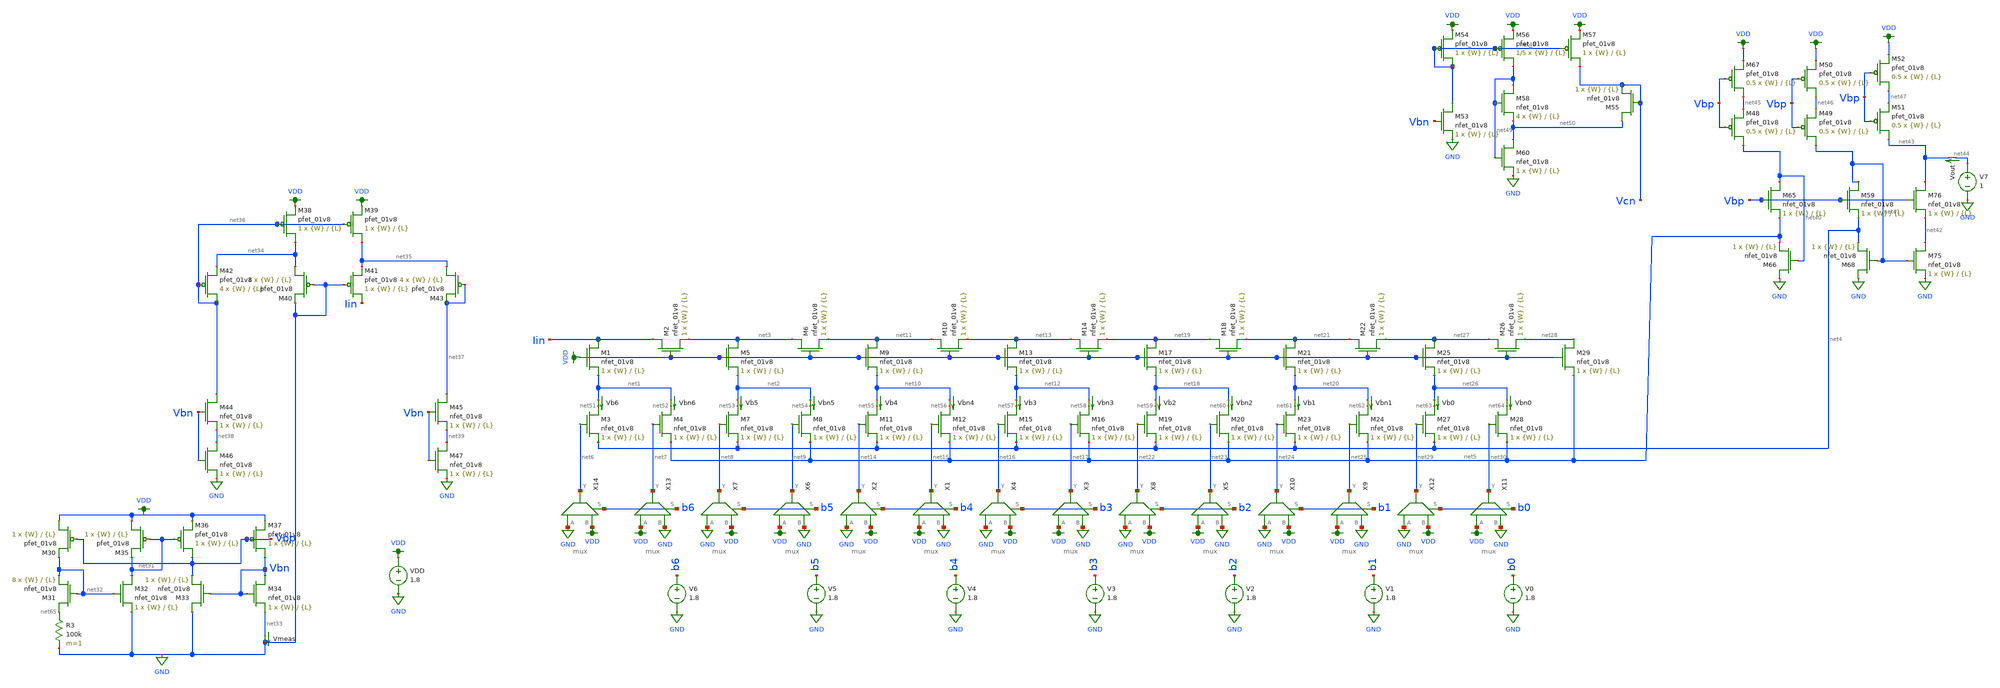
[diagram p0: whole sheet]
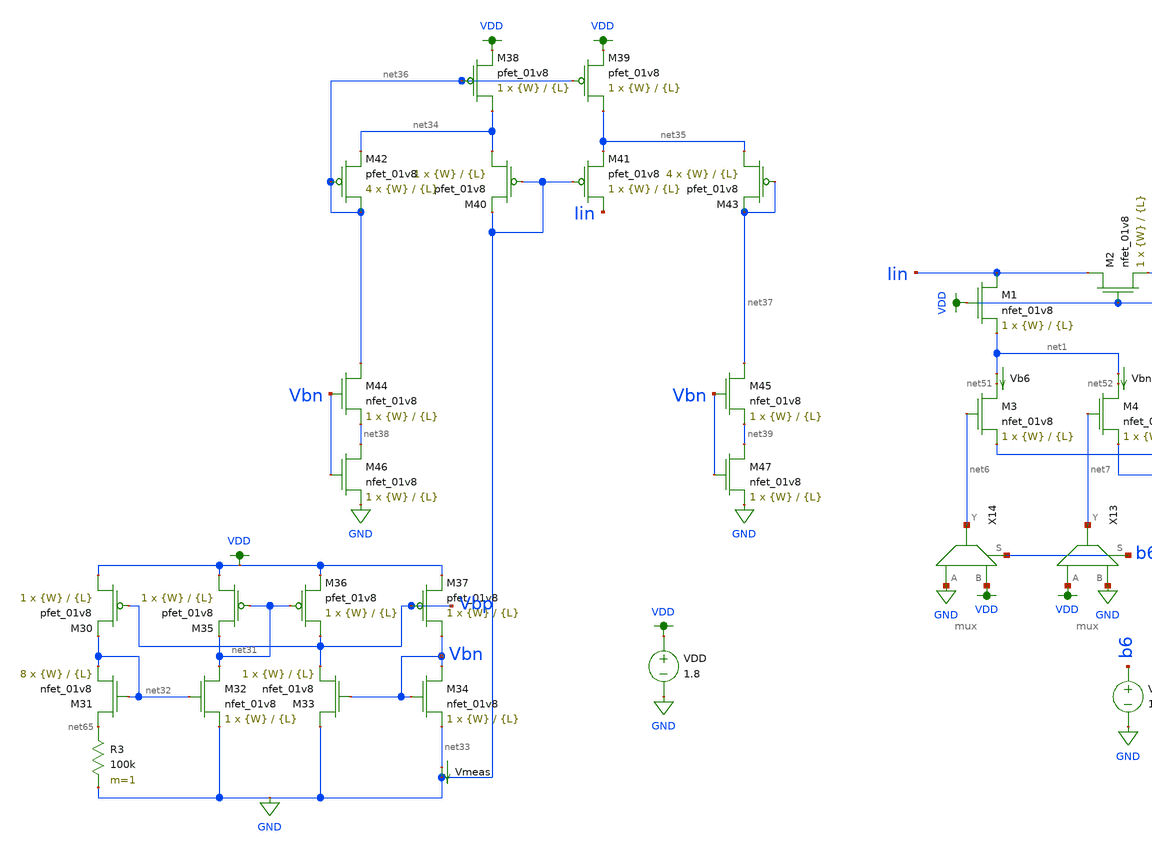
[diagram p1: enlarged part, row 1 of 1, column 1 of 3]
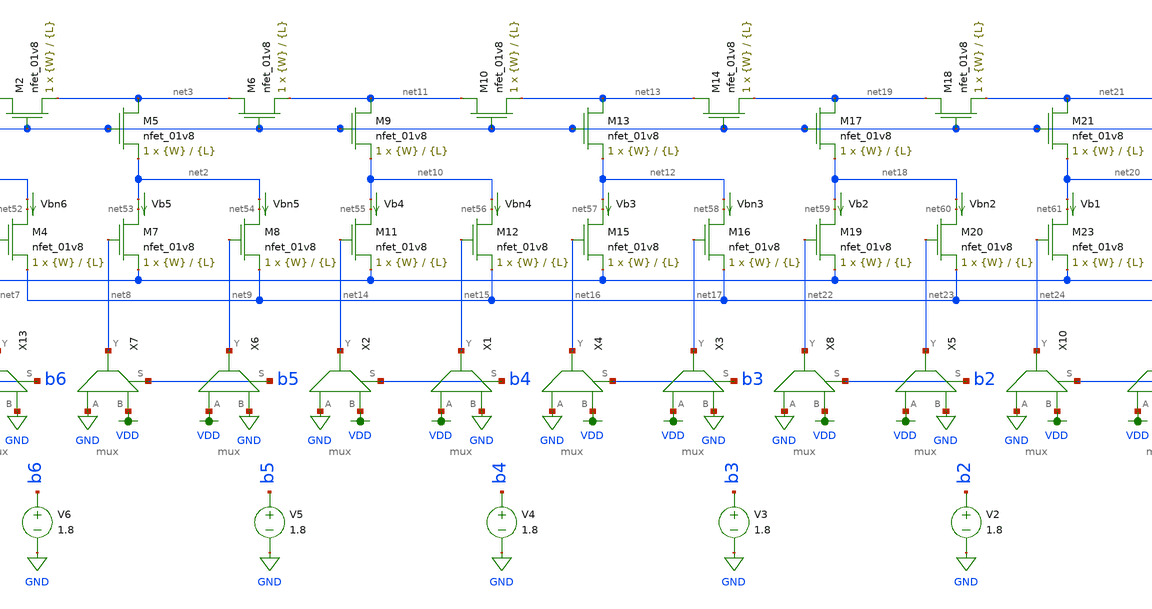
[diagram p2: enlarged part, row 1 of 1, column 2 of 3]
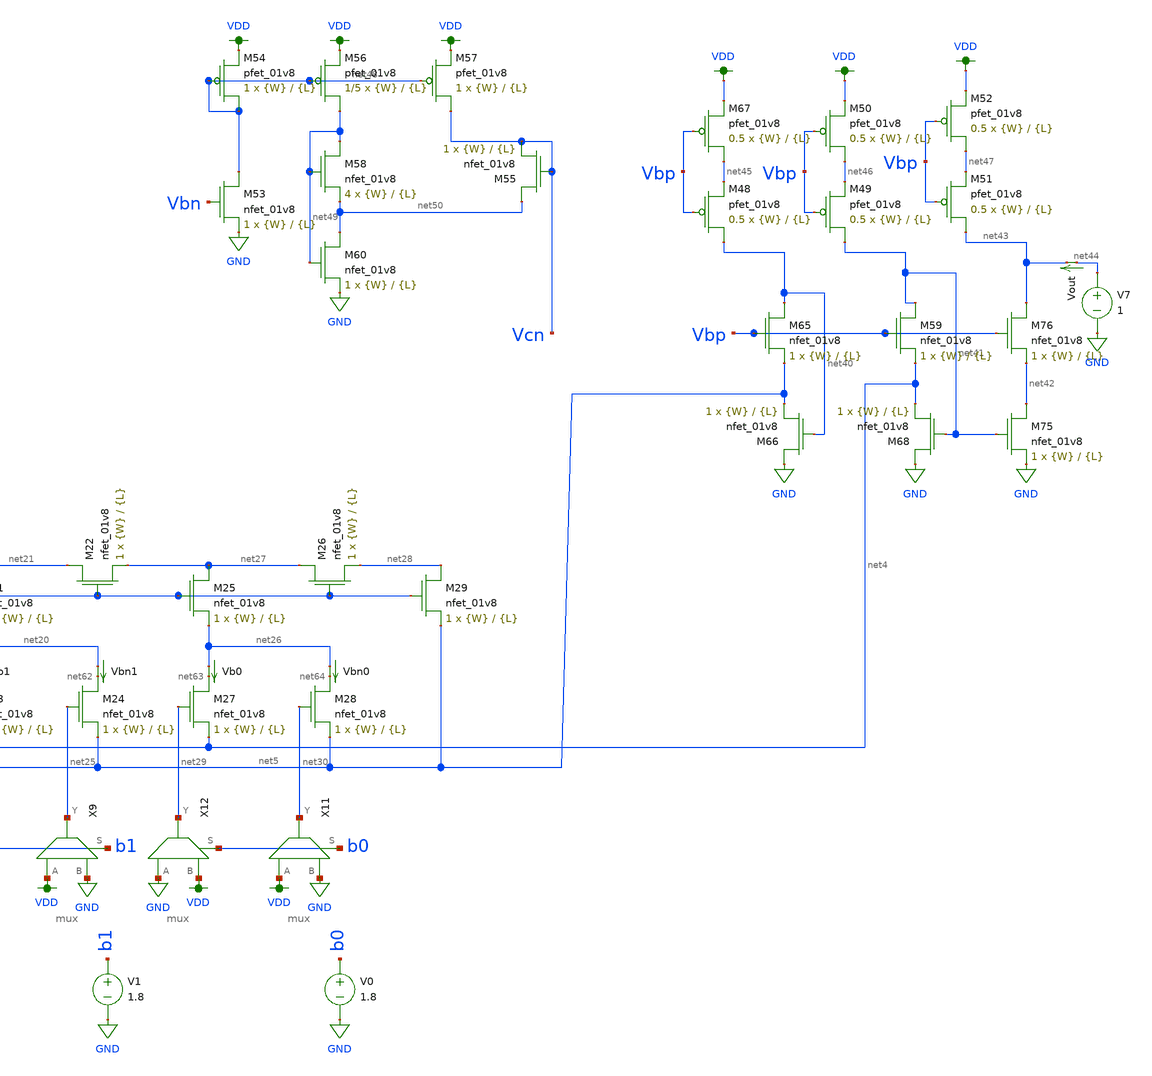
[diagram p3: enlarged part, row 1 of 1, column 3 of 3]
** sch_path: schematics/dac_from_paper_2.sch
**.subckt dac_from_paper_2
XM1 Iin VDD net1 GND sky130_fd_pr__nfet_01v8 L={L} W={W} nf=1 ad='int((nf+1)/2) * W/nf * 0.29' as='int((nf+2)/2) * W/nf * 0.29'
+ pd='2*int((nf+1)/2) * (W/nf + 0.29)' ps='2*int((nf+2)/2) * (W/nf + 0.29)' nrd='0.29 / W' nrs='0.29 / W'
+ sa=0 sb=0 sd=0 mult=1 m=1
XM2 Iin VDD net3 GND sky130_fd_pr__nfet_01v8 L={L} W={W} nf=1 ad='int((nf+1)/2) * W/nf * 0.29' as='int((nf+2)/2) * W/nf * 0.29'
+ pd='2*int((nf+1)/2) * (W/nf + 0.29)' ps='2*int((nf+2)/2) * (W/nf + 0.29)' nrd='0.29 / W' nrs='0.29 / W'
+ sa=0 sb=0 sd=0 mult=1 m=1
XM3 net51 net6 net4 GND sky130_fd_pr__nfet_01v8 L={L} W={W} nf=1 ad='int((nf+1)/2) * W/nf * 0.29' as='int((nf+2)/2) * W/nf * 0.29'
+ pd='2*int((nf+1)/2) * (W/nf + 0.29)' ps='2*int((nf+2)/2) * (W/nf + 0.29)' nrd='0.29 / W' nrs='0.29 / W'
+ sa=0 sb=0 sd=0 mult=1 m=1
XM4 net52 net7 net5 GND sky130_fd_pr__nfet_01v8 L={L} W={W} nf=1 ad='int((nf+1)/2) * W/nf * 0.29' as='int((nf+2)/2) * W/nf * 0.29'
+ pd='2*int((nf+1)/2) * (W/nf + 0.29)' ps='2*int((nf+2)/2) * (W/nf + 0.29)' nrd='0.29 / W' nrs='0.29 / W'
+ sa=0 sb=0 sd=0 mult=1 m=1
XM5 net3 VDD net2 GND sky130_fd_pr__nfet_01v8 L={L} W={W} nf=1 ad='int((nf+1)/2) * W/nf * 0.29' as='int((nf+2)/2) * W/nf * 0.29'
+ pd='2*int((nf+1)/2) * (W/nf + 0.29)' ps='2*int((nf+2)/2) * (W/nf + 0.29)' nrd='0.29 / W' nrs='0.29 / W'
+ sa=0 sb=0 sd=0 mult=1 m=1
XM6 net3 VDD net11 GND sky130_fd_pr__nfet_01v8 L={L} W={W} nf=1 ad='int((nf+1)/2) * W/nf * 0.29' as='int((nf+2)/2) * W/nf * 0.29'
+ pd='2*int((nf+1)/2) * (W/nf + 0.29)' ps='2*int((nf+2)/2) * (W/nf + 0.29)' nrd='0.29 / W' nrs='0.29 / W'
+ sa=0 sb=0 sd=0 mult=1 m=1
XM7 net53 net8 net4 GND sky130_fd_pr__nfet_01v8 L={L} W={W} nf=1 ad='int((nf+1)/2) * W/nf * 0.29' as='int((nf+2)/2) * W/nf * 0.29'
+ pd='2*int((nf+1)/2) * (W/nf + 0.29)' ps='2*int((nf+2)/2) * (W/nf + 0.29)' nrd='0.29 / W' nrs='0.29 / W'
+ sa=0 sb=0 sd=0 mult=1 m=1
XM8 net54 net9 net5 GND sky130_fd_pr__nfet_01v8 L={L} W={W} nf=1 ad='int((nf+1)/2) * W/nf * 0.29' as='int((nf+2)/2) * W/nf * 0.29'
+ pd='2*int((nf+1)/2) * (W/nf + 0.29)' ps='2*int((nf+2)/2) * (W/nf + 0.29)' nrd='0.29 / W' nrs='0.29 / W'
+ sa=0 sb=0 sd=0 mult=1 m=1
XM9 net11 VDD net10 GND sky130_fd_pr__nfet_01v8 L={L} W={W} nf=1 ad='int((nf+1)/2) * W/nf * 0.29' as='int((nf+2)/2) * W/nf * 0.29'
+ pd='2*int((nf+1)/2) * (W/nf + 0.29)' ps='2*int((nf+2)/2) * (W/nf + 0.29)' nrd='0.29 / W' nrs='0.29 / W'
+ sa=0 sb=0 sd=0 mult=1 m=1
XM10 net11 VDD net13 GND sky130_fd_pr__nfet_01v8 L={L} W={W} nf=1 ad='int((nf+1)/2) * W/nf * 0.29' as='int((nf+2)/2) * W/nf * 0.29'
+ pd='2*int((nf+1)/2) * (W/nf + 0.29)' ps='2*int((nf+2)/2) * (W/nf + 0.29)' nrd='0.29 / W' nrs='0.29 / W'
+ sa=0 sb=0 sd=0 mult=1 m=1
XM11 net55 net14 net4 GND sky130_fd_pr__nfet_01v8 L={L} W={W} nf=1 ad='int((nf+1)/2) * W/nf * 0.29' as='int((nf+2)/2) * W/nf * 0.29'
+ pd='2*int((nf+1)/2) * (W/nf + 0.29)' ps='2*int((nf+2)/2) * (W/nf + 0.29)' nrd='0.29 / W' nrs='0.29 / W'
+ sa=0 sb=0 sd=0 mult=1 m=1
XM12 net56 net15 net5 GND sky130_fd_pr__nfet_01v8 L={L} W={W} nf=1 ad='int((nf+1)/2) * W/nf * 0.29' as='int((nf+2)/2) * W/nf * 0.29'
+ pd='2*int((nf+1)/2) * (W/nf + 0.29)' ps='2*int((nf+2)/2) * (W/nf + 0.29)' nrd='0.29 / W' nrs='0.29 / W'
+ sa=0 sb=0 sd=0 mult=1 m=1
XM13 net13 VDD net12 GND sky130_fd_pr__nfet_01v8 L={L} W={W} nf=1 ad='int((nf+1)/2) * W/nf * 0.29' as='int((nf+2)/2) * W/nf * 0.29'
+ pd='2*int((nf+1)/2) * (W/nf + 0.29)' ps='2*int((nf+2)/2) * (W/nf + 0.29)' nrd='0.29 / W' nrs='0.29 / W'
+ sa=0 sb=0 sd=0 mult=1 m=1
XM14 net13 VDD net19 GND sky130_fd_pr__nfet_01v8 L={L} W={W} nf=1 ad='int((nf+1)/2) * W/nf * 0.29' as='int((nf+2)/2) * W/nf * 0.29'
+ pd='2*int((nf+1)/2) * (W/nf + 0.29)' ps='2*int((nf+2)/2) * (W/nf + 0.29)' nrd='0.29 / W' nrs='0.29 / W'
+ sa=0 sb=0 sd=0 mult=1 m=1
XM15 net57 net16 net4 GND sky130_fd_pr__nfet_01v8 L={L} W={W} nf=1 ad='int((nf+1)/2) * W/nf * 0.29' as='int((nf+2)/2) * W/nf * 0.29'
+ pd='2*int((nf+1)/2) * (W/nf + 0.29)' ps='2*int((nf+2)/2) * (W/nf + 0.29)' nrd='0.29 / W' nrs='0.29 / W'
+ sa=0 sb=0 sd=0 mult=1 m=1
XM16 net58 net17 net5 GND sky130_fd_pr__nfet_01v8 L={L} W={W} nf=1 ad='int((nf+1)/2) * W/nf * 0.29' as='int((nf+2)/2) * W/nf * 0.29'
+ pd='2*int((nf+1)/2) * (W/nf + 0.29)' ps='2*int((nf+2)/2) * (W/nf + 0.29)' nrd='0.29 / W' nrs='0.29 / W'
+ sa=0 sb=0 sd=0 mult=1 m=1
XM17 net19 VDD net18 GND sky130_fd_pr__nfet_01v8 L={L} W={W} nf=1 ad='int((nf+1)/2) * W/nf * 0.29' as='int((nf+2)/2) * W/nf * 0.29'
+ pd='2*int((nf+1)/2) * (W/nf + 0.29)' ps='2*int((nf+2)/2) * (W/nf + 0.29)' nrd='0.29 / W' nrs='0.29 / W'
+ sa=0 sb=0 sd=0 mult=1 m=1
XM18 net19 VDD net21 GND sky130_fd_pr__nfet_01v8 L={L} W={W} nf=1 ad='int((nf+1)/2) * W/nf * 0.29' as='int((nf+2)/2) * W/nf * 0.29'
+ pd='2*int((nf+1)/2) * (W/nf + 0.29)' ps='2*int((nf+2)/2) * (W/nf + 0.29)' nrd='0.29 / W' nrs='0.29 / W'
+ sa=0 sb=0 sd=0 mult=1 m=1
XM19 net59 net22 net4 GND sky130_fd_pr__nfet_01v8 L={L} W={W} nf=1 ad='int((nf+1)/2) * W/nf * 0.29' as='int((nf+2)/2) * W/nf * 0.29'
+ pd='2*int((nf+1)/2) * (W/nf + 0.29)' ps='2*int((nf+2)/2) * (W/nf + 0.29)' nrd='0.29 / W' nrs='0.29 / W'
+ sa=0 sb=0 sd=0 mult=1 m=1
XM20 net60 net23 net5 GND sky130_fd_pr__nfet_01v8 L={L} W={W} nf=1 ad='int((nf+1)/2) * W/nf * 0.29' as='int((nf+2)/2) * W/nf * 0.29'
+ pd='2*int((nf+1)/2) * (W/nf + 0.29)' ps='2*int((nf+2)/2) * (W/nf + 0.29)' nrd='0.29 / W' nrs='0.29 / W'
+ sa=0 sb=0 sd=0 mult=1 m=1
XM21 net21 VDD net20 GND sky130_fd_pr__nfet_01v8 L={L} W={W} nf=1 ad='int((nf+1)/2) * W/nf * 0.29' as='int((nf+2)/2) * W/nf * 0.29'
+ pd='2*int((nf+1)/2) * (W/nf + 0.29)' ps='2*int((nf+2)/2) * (W/nf + 0.29)' nrd='0.29 / W' nrs='0.29 / W'
+ sa=0 sb=0 sd=0 mult=1 m=1
XM22 net21 VDD net27 GND sky130_fd_pr__nfet_01v8 L={L} W={W} nf=1 ad='int((nf+1)/2) * W/nf * 0.29' as='int((nf+2)/2) * W/nf * 0.29'
+ pd='2*int((nf+1)/2) * (W/nf + 0.29)' ps='2*int((nf+2)/2) * (W/nf + 0.29)' nrd='0.29 / W' nrs='0.29 / W'
+ sa=0 sb=0 sd=0 mult=1 m=1
XM23 net61 net24 net4 GND sky130_fd_pr__nfet_01v8 L={L} W={W} nf=1 ad='int((nf+1)/2) * W/nf * 0.29' as='int((nf+2)/2) * W/nf * 0.29'
+ pd='2*int((nf+1)/2) * (W/nf + 0.29)' ps='2*int((nf+2)/2) * (W/nf + 0.29)' nrd='0.29 / W' nrs='0.29 / W'
+ sa=0 sb=0 sd=0 mult=1 m=1
XM24 net62 net25 net5 GND sky130_fd_pr__nfet_01v8 L={L} W={W} nf=1 ad='int((nf+1)/2) * W/nf * 0.29' as='int((nf+2)/2) * W/nf * 0.29'
+ pd='2*int((nf+1)/2) * (W/nf + 0.29)' ps='2*int((nf+2)/2) * (W/nf + 0.29)' nrd='0.29 / W' nrs='0.29 / W'
+ sa=0 sb=0 sd=0 mult=1 m=1
XM25 net27 VDD net26 GND sky130_fd_pr__nfet_01v8 L={L} W={W} nf=1 ad='int((nf+1)/2) * W/nf * 0.29' as='int((nf+2)/2) * W/nf * 0.29'
+ pd='2*int((nf+1)/2) * (W/nf + 0.29)' ps='2*int((nf+2)/2) * (W/nf + 0.29)' nrd='0.29 / W' nrs='0.29 / W'
+ sa=0 sb=0 sd=0 mult=1 m=1
XM26 net27 VDD net28 GND sky130_fd_pr__nfet_01v8 L={L} W={W} nf=1 ad='int((nf+1)/2) * W/nf * 0.29' as='int((nf+2)/2) * W/nf * 0.29'
+ pd='2*int((nf+1)/2) * (W/nf + 0.29)' ps='2*int((nf+2)/2) * (W/nf + 0.29)' nrd='0.29 / W' nrs='0.29 / W'
+ sa=0 sb=0 sd=0 mult=1 m=1
XM27 net63 net29 net4 GND sky130_fd_pr__nfet_01v8 L={L} W={W} nf=1 ad='int((nf+1)/2) * W/nf * 0.29' as='int((nf+2)/2) * W/nf * 0.29'
+ pd='2*int((nf+1)/2) * (W/nf + 0.29)' ps='2*int((nf+2)/2) * (W/nf + 0.29)' nrd='0.29 / W' nrs='0.29 / W'
+ sa=0 sb=0 sd=0 mult=1 m=1
XM28 net64 net30 net5 GND sky130_fd_pr__nfet_01v8 L={L} W={W} nf=1 ad='int((nf+1)/2) * W/nf * 0.29' as='int((nf+2)/2) * W/nf * 0.29'
+ pd='2*int((nf+1)/2) * (W/nf + 0.29)' ps='2*int((nf+2)/2) * (W/nf + 0.29)' nrd='0.29 / W' nrs='0.29 / W'
+ sa=0 sb=0 sd=0 mult=1 m=1
XM29 net28 VDD net5 GND sky130_fd_pr__nfet_01v8 L={L} W={W} nf=1 ad='int((nf+1)/2) * W/nf * 0.29' as='int((nf+2)/2) * W/nf * 0.29'
+ pd='2*int((nf+1)/2) * (W/nf + 0.29)' ps='2*int((nf+2)/2) * (W/nf + 0.29)' nrd='0.29 / W' nrs='0.29 / W'
+ sa=0 sb=0 sd=0 mult=1 m=1
Vb0 net26 net63 0
.save i(vb0)
Vbn0 net26 net64 0
.save i(vbn0)
Vb5 net2 net53 0
.save i(vb5)
Vb6 net1 net51 0
.save i(vb6)
Vb1 net20 net61 0
.save i(vb1)
Vb2 net18 net59 0
.save i(vb2)
Vb3 net12 net57 0
.save i(vb3)
Vb4 net10 net55 0
.save i(vb4)
Vbn1 net20 net62 0
.save i(vbn1)
Vbn2 net18 net60 0
.save i(vbn2)
Vbn3 net12 net58 0
.save i(vbn3)
Vbn4 net10 net56 0
.save i(vbn4)
Vbn5 net2 net54 0
.save i(vbn5)
Vbn6 net1 net52 0
.save i(vbn6)
V0 b0 GND 1.8
V1 b1 GND 1.8
V2 b2 GND 1.8
V3 b3 GND 1.8
V4 b4 GND 1.8
V5 b5 GND 1.8
V6 b6 GND 1.8
XM30 VDD Vbp net32 VDD sky130_fd_pr__pfet_01v8 L={L} W={W} nf=1 ad='int((nf+1)/2) * W/nf * 0.29' as='int((nf+2)/2) * W/nf * 0.29'
+ pd='2*int((nf+1)/2) * (W/nf + 0.29)' ps='2*int((nf+2)/2) * (W/nf + 0.29)' nrd='0.29 / W' nrs='0.29 / W'
+ sa=0 sb=0 sd=0 mult=1 m=1
XM31 net65 net32 net32 GND sky130_fd_pr__nfet_01v8 L={L} W={W} nf=1 ad='int((nf+1)/2) * W/nf * 0.29'
+ as='int((nf+2)/2) * W/nf * 0.29' pd='2*int((nf+1)/2) * (W/nf + 0.29)' ps='2*int((nf+2)/2) * (W/nf + 0.29)'
+ nrd='0.29 / W' nrs='0.29 / W' sa=0 sb=0 sd=0 mult=8 m=8
R3 net65 GND 100k m=1
XM32 net31 net32 GND GND sky130_fd_pr__nfet_01v8 L={L} W={W} nf=1 ad='int((nf+1)/2) * W/nf * 0.29' as='int((nf+2)/2) * W/nf * 0.29'
+ pd='2*int((nf+1)/2) * (W/nf + 0.29)' ps='2*int((nf+2)/2) * (W/nf + 0.29)' nrd='0.29 / W' nrs='0.29 / W'
+ sa=0 sb=0 sd=0 mult=1 m=1
XM33 GND Vbn Vbp GND sky130_fd_pr__nfet_01v8 L={L} W={W} nf=1 ad='int((nf+1)/2) * W/nf * 0.29' as='int((nf+2)/2) * W/nf * 0.29'
+ pd='2*int((nf+1)/2) * (W/nf + 0.29)' ps='2*int((nf+2)/2) * (W/nf + 0.29)' nrd='0.29 / W' nrs='0.29 / W'
+ sa=0 sb=0 sd=0 mult=1 m=1
XM34 Vbn Vbn net33 GND sky130_fd_pr__nfet_01v8 L={L} W={W} nf=1 ad='int((nf+1)/2) * W/nf * 0.29' as='int((nf+2)/2) * W/nf * 0.29'
+ pd='2*int((nf+1)/2) * (W/nf + 0.29)' ps='2*int((nf+2)/2) * (W/nf + 0.29)' nrd='0.29 / W' nrs='0.29 / W'
+ sa=0 sb=0 sd=0 mult=1 m=1
XM35 VDD net31 net31 VDD sky130_fd_pr__pfet_01v8 L={L} W={W} nf=1 ad='int((nf+1)/2) * W/nf * 0.29' as='int((nf+2)/2) * W/nf * 0.29'
+ pd='2*int((nf+1)/2) * (W/nf + 0.29)' ps='2*int((nf+2)/2) * (W/nf + 0.29)' nrd='0.29 / W' nrs='0.29 / W'
+ sa=0 sb=0 sd=0 mult=1 m=1
XM36 Vbp net31 VDD VDD sky130_fd_pr__pfet_01v8 L={L} W={W} nf=1 ad='int((nf+1)/2) * W/nf * 0.29' as='int((nf+2)/2) * W/nf * 0.29'
+ pd='2*int((nf+1)/2) * (W/nf + 0.29)' ps='2*int((nf+2)/2) * (W/nf + 0.29)' nrd='0.29 / W' nrs='0.29 / W'
+ sa=0 sb=0 sd=0 mult=1 m=1
XM37 Vbn Vbp VDD VDD sky130_fd_pr__pfet_01v8 L={L} W={W} nf=1 ad='int((nf+1)/2) * W/nf * 0.29' as='int((nf+2)/2) * W/nf * 0.29'
+ pd='2*int((nf+1)/2) * (W/nf + 0.29)' ps='2*int((nf+2)/2) * (W/nf + 0.29)' nrd='0.29 / W' nrs='0.29 / W'
+ sa=0 sb=0 sd=0 mult=1 m=1
VDD VDD GND 1.8
Vmeas net33 GND 0
.save i(vmeas)
X13 VDD GND net7 b6 mux
X14 GND VDD net6 b6 mux
X6 VDD GND net9 b5 mux
X7 GND VDD net8 b5 mux
X1 VDD GND net15 b4 mux
X2 GND VDD net14 b4 mux
X3 VDD GND net17 b3 mux
X4 GND VDD net16 b3 mux
X5 VDD GND net23 b2 mux
X8 GND VDD net22 b2 mux
X9 VDD GND net25 b1 mux
X10 GND VDD net24 b1 mux
X11 VDD GND net30 b0 mux
X12 GND VDD net29 b0 mux
XM38 net34 net36 VDD VDD sky130_fd_pr__pfet_01v8 L={L} W={W} nf=1 ad='int((nf+1)/2) * W/nf * 0.29' as='int((nf+2)/2) * W/nf * 0.29'
+ pd='2*int((nf+1)/2) * (W/nf + 0.29)' ps='2*int((nf+2)/2) * (W/nf + 0.29)' nrd='0.29 / W' nrs='0.29 / W'
+ sa=0 sb=0 sd=0 mult=1 m=1
XM39 net35 net36 VDD VDD sky130_fd_pr__pfet_01v8 L={L} W={W} nf=1 ad='int((nf+1)/2) * W/nf * 0.29' as='int((nf+2)/2) * W/nf * 0.29'
+ pd='2*int((nf+1)/2) * (W/nf + 0.29)' ps='2*int((nf+2)/2) * (W/nf + 0.29)' nrd='0.29 / W' nrs='0.29 / W'
+ sa=0 sb=0 sd=0 mult=1 m=1
XM40 net34 GND GND VDD sky130_fd_pr__pfet_01v8 L={L} W={W} nf=1 ad='int((nf+1)/2) * W/nf * 0.29' as='int((nf+2)/2) * W/nf * 0.29'
+ pd='2*int((nf+1)/2) * (W/nf + 0.29)' ps='2*int((nf+2)/2) * (W/nf + 0.29)' nrd='0.29 / W' nrs='0.29 / W'
+ sa=0 sb=0 sd=0 mult=1 m=1
XM41 Iin GND net35 VDD sky130_fd_pr__pfet_01v8 L={L} W={W} nf=1 ad='int((nf+1)/2) * W/nf * 0.29' as='int((nf+2)/2) * W/nf * 0.29'
+ pd='2*int((nf+1)/2) * (W/nf + 0.29)' ps='2*int((nf+2)/2) * (W/nf + 0.29)' nrd='0.29 / W' nrs='0.29 / W'
+ sa=0 sb=0 sd=0 mult=1 m=1
XM42 net36 net36 net34 VDD sky130_fd_pr__pfet_01v8 L={L} W={W} nf=1 ad='int((nf+1)/2) * W/nf * 0.29'
+ as='int((nf+2)/2) * W/nf * 0.29' pd='2*int((nf+1)/2) * (W/nf + 0.29)' ps='2*int((nf+2)/2) * (W/nf + 0.29)'
+ nrd='0.29 / W' nrs='0.29 / W' sa=0 sb=0 sd=0 mult=4 m=4
XM43 net35 net37 net37 VDD sky130_fd_pr__pfet_01v8 L={L} W={W} nf=1 ad='int((nf+1)/2) * W/nf * 0.29'
+ as='int((nf+2)/2) * W/nf * 0.29' pd='2*int((nf+1)/2) * (W/nf + 0.29)' ps='2*int((nf+2)/2) * (W/nf + 0.29)'
+ nrd='0.29 / W' nrs='0.29 / W' sa=0 sb=0 sd=0 mult=4 m=4
XM44 net36 Vbn net38 GND sky130_fd_pr__nfet_01v8 L={L} W={W} nf=1 ad='int((nf+1)/2) * W/nf * 0.29' as='int((nf+2)/2) * W/nf * 0.29'
+ pd='2*int((nf+1)/2) * (W/nf + 0.29)' ps='2*int((nf+2)/2) * (W/nf + 0.29)' nrd='0.29 / W' nrs='0.29 / W'
+ sa=0 sb=0 sd=0 mult=1 m=1
XM45 net37 Vbn net39 GND sky130_fd_pr__nfet_01v8 L={L} W={W} nf=1 ad='int((nf+1)/2) * W/nf * 0.29' as='int((nf+2)/2) * W/nf * 0.29'
+ pd='2*int((nf+1)/2) * (W/nf + 0.29)' ps='2*int((nf+2)/2) * (W/nf + 0.29)' nrd='0.29 / W' nrs='0.29 / W'
+ sa=0 sb=0 sd=0 mult=1 m=1
XM46 net38 Vbn GND GND sky130_fd_pr__nfet_01v8 L={L} W={W} nf=1 ad='int((nf+1)/2) * W/nf * 0.29' as='int((nf+2)/2) * W/nf * 0.29'
+ pd='2*int((nf+1)/2) * (W/nf + 0.29)' ps='2*int((nf+2)/2) * (W/nf + 0.29)' nrd='0.29 / W' nrs='0.29 / W'
+ sa=0 sb=0 sd=0 mult=1 m=1
XM47 net39 Vbn GND GND sky130_fd_pr__nfet_01v8 L={L} W={W} nf=1 ad='int((nf+1)/2) * W/nf * 0.29' as='int((nf+2)/2) * W/nf * 0.29'
+ pd='2*int((nf+1)/2) * (W/nf + 0.29)' ps='2*int((nf+2)/2) * (W/nf + 0.29)' nrd='0.29 / W' nrs='0.29 / W'
+ sa=0 sb=0 sd=0 mult=1 m=1
XM65 net40 Vbp net5 GND sky130_fd_pr__nfet_01v8 L={L} W={W} nf=1 ad='int((nf+1)/2) * W/nf * 0.29' as='int((nf+2)/2) * W/nf * 0.29'
+ pd='2*int((nf+1)/2) * (W/nf + 0.29)' ps='2*int((nf+2)/2) * (W/nf + 0.29)' nrd='0.29 / W' nrs='0.29 / W'
+ sa=0 sb=0 sd=0 mult=1 m=1
XM66 GND net40 net5 GND sky130_fd_pr__nfet_01v8 L={L} W={W} nf=1 ad='int((nf+1)/2) * W/nf * 0.29' as='int((nf+2)/2) * W/nf * 0.29'
+ pd='2*int((nf+1)/2) * (W/nf + 0.29)' ps='2*int((nf+2)/2) * (W/nf + 0.29)' nrd='0.29 / W' nrs='0.29 / W'
+ sa=0 sb=0 sd=0 mult=1 m=1
XM59 net41 Vbp net4 GND sky130_fd_pr__nfet_01v8 L={L} W={W} nf=1 ad='int((nf+1)/2) * W/nf * 0.29' as='int((nf+2)/2) * W/nf * 0.29'
+ pd='2*int((nf+1)/2) * (W/nf + 0.29)' ps='2*int((nf+2)/2) * (W/nf + 0.29)' nrd='0.29 / W' nrs='0.29 / W'
+ sa=0 sb=0 sd=0 mult=1 m=1
XM68 GND net41 net4 GND sky130_fd_pr__nfet_01v8 L={L} W={W} nf=1 ad='int((nf+1)/2) * W/nf * 0.29' as='int((nf+2)/2) * W/nf * 0.29'
+ pd='2*int((nf+1)/2) * (W/nf + 0.29)' ps='2*int((nf+2)/2) * (W/nf + 0.29)' nrd='0.29 / W' nrs='0.29 / W'
+ sa=0 sb=0 sd=0 mult=1 m=1
XM75 net42 net41 GND GND sky130_fd_pr__nfet_01v8 L={L} W={W} nf=1 ad='int((nf+1)/2) * W/nf * 0.29' as='int((nf+2)/2) * W/nf * 0.29'
+ pd='2*int((nf+1)/2) * (W/nf + 0.29)' ps='2*int((nf+2)/2) * (W/nf + 0.29)' nrd='0.29 / W' nrs='0.29 / W'
+ sa=0 sb=0 sd=0 mult=1 m=1
XM76 net43 Vbp net42 GND sky130_fd_pr__nfet_01v8 L={L} W={W} nf=1 ad='int((nf+1)/2) * W/nf * 0.29' as='int((nf+2)/2) * W/nf * 0.29'
+ pd='2*int((nf+1)/2) * (W/nf + 0.29)' ps='2*int((nf+2)/2) * (W/nf + 0.29)' nrd='0.29 / W' nrs='0.29 / W'
+ sa=0 sb=0 sd=0 mult=1 m=1
Vout net44 net43 0
.save i(vout)
V7 net44 GND 1
XM48 net40 Vbp net45 VDD sky130_fd_pr__pfet_01v8 L={L} W={W} nf=1 ad='int((nf+1)/2) * W/nf * 0.29' as='int((nf+2)/2) * W/nf * 0.29'
+ pd='2*int((nf+1)/2) * (W/nf + 0.29)' ps='2*int((nf+2)/2) * (W/nf + 0.29)' nrd='0.29 / W' nrs='0.29 / W'
+ sa=0 sb=0 sd=0 mult=0.5 m=0.5
XM67 net45 Vbp VDD VDD sky130_fd_pr__pfet_01v8 L={L} W={W} nf=1 ad='int((nf+1)/2) * W/nf * 0.29' as='int((nf+2)/2) * W/nf * 0.29'
+ pd='2*int((nf+1)/2) * (W/nf + 0.29)' ps='2*int((nf+2)/2) * (W/nf + 0.29)' nrd='0.29 / W' nrs='0.29 / W'
+ sa=0 sb=0 sd=0 mult=0.5 m=0.5
XM49 net41 Vbp net46 VDD sky130_fd_pr__pfet_01v8 L={L} W={W} nf=1 ad='int((nf+1)/2) * W/nf * 0.29' as='int((nf+2)/2) * W/nf * 0.29'
+ pd='2*int((nf+1)/2) * (W/nf + 0.29)' ps='2*int((nf+2)/2) * (W/nf + 0.29)' nrd='0.29 / W' nrs='0.29 / W'
+ sa=0 sb=0 sd=0 mult=0.5 m=0.5
XM50 net46 Vbp VDD VDD sky130_fd_pr__pfet_01v8 L={L} W={W} nf=1 ad='int((nf+1)/2) * W/nf * 0.29' as='int((nf+2)/2) * W/nf * 0.29'
+ pd='2*int((nf+1)/2) * (W/nf + 0.29)' ps='2*int((nf+2)/2) * (W/nf + 0.29)' nrd='0.29 / W' nrs='0.29 / W'
+ sa=0 sb=0 sd=0 mult=0.5 m=0.5
XM51 net43 Vbp net47 VDD sky130_fd_pr__pfet_01v8 L={L} W={W} nf=1 ad='int((nf+1)/2) * W/nf * 0.29' as='int((nf+2)/2) * W/nf * 0.29'
+ pd='2*int((nf+1)/2) * (W/nf + 0.29)' ps='2*int((nf+2)/2) * (W/nf + 0.29)' nrd='0.29 / W' nrs='0.29 / W'
+ sa=0 sb=0 sd=0 mult=0.5 m=0.5
XM52 net47 Vbp VDD VDD sky130_fd_pr__pfet_01v8 L={L} W={W} nf=1 ad='int((nf+1)/2) * W/nf * 0.29' as='int((nf+2)/2) * W/nf * 0.29'
+ pd='2*int((nf+1)/2) * (W/nf + 0.29)' ps='2*int((nf+2)/2) * (W/nf + 0.29)' nrd='0.29 / W' nrs='0.29 / W'
+ sa=0 sb=0 sd=0 mult=0.5 m=0.5
XM53 net48 Vbn GND GND sky130_fd_pr__nfet_01v8 L={L} W={W} nf=1 ad='int((nf+1)/2) * W/nf * 0.29' as='int((nf+2)/2) * W/nf * 0.29'
+ pd='2*int((nf+1)/2) * (W/nf + 0.29)' ps='2*int((nf+2)/2) * (W/nf + 0.29)' nrd='0.29 / W' nrs='0.29 / W'
+ sa=0 sb=0 sd=0 mult=1 m=1
XM54 net48 net48 VDD VDD sky130_fd_pr__pfet_01v8 L={L} W={W} nf=1 ad='int((nf+1)/2) * W/nf * 0.29' as='int((nf+2)/2) * W/nf * 0.29'
+ pd='2*int((nf+1)/2) * (W/nf + 0.29)' ps='2*int((nf+2)/2) * (W/nf + 0.29)' nrd='0.29 / W' nrs='0.29 / W'
+ sa=0 sb=0 sd=0 mult=1 m=1
XM55 net50 Vcn Vcn GND sky130_fd_pr__nfet_01v8 L={L} W={W} nf=1 ad='int((nf+1)/2) * W/nf * 0.29' as='int((nf+2)/2) * W/nf * 0.29'
+ pd='2*int((nf+1)/2) * (W/nf + 0.29)' ps='2*int((nf+2)/2) * (W/nf + 0.29)' nrd='0.29 / W' nrs='0.29 / W'
+ sa=0 sb=0 sd=0 mult=1 m=1
XM56 net49 net48 VDD VDD sky130_fd_pr__pfet_01v8 L={L} W={W} nf=1 ad='int((nf+1)/2) * W/nf * 0.29' as='int((nf+2)/2) * W/nf * 0.29'
+ pd='2*int((nf+1)/2) * (W/nf + 0.29)' ps='2*int((nf+2)/2) * (W/nf + 0.29)' nrd='0.29 / W' nrs='0.29 / W'
+ sa=0 sb=0 sd=0 mult=1/5 m=1/5
XM57 Vcn net48 VDD VDD sky130_fd_pr__pfet_01v8 L={L} W={W} nf=1 ad='int((nf+1)/2) * W/nf * 0.29' as='int((nf+2)/2) * W/nf * 0.29'
+ pd='2*int((nf+1)/2) * (W/nf + 0.29)' ps='2*int((nf+2)/2) * (W/nf + 0.29)' nrd='0.29 / W' nrs='0.29 / W'
+ sa=0 sb=0 sd=0 mult=1 m=1
XM58 net49 net49 net50 GND sky130_fd_pr__nfet_01v8 L={L} W={W} nf=1 ad='int((nf+1)/2) * W/nf * 0.29'
+ as='int((nf+2)/2) * W/nf * 0.29' pd='2*int((nf+1)/2) * (W/nf + 0.29)' ps='2*int((nf+2)/2) * (W/nf + 0.29)'
+ nrd='0.29 / W' nrs='0.29 / W' sa=0 sb=0 sd=0 mult=4 m=4
XM60 net50 net49 GND GND sky130_fd_pr__nfet_01v8 L={L} W={W} nf=1 ad='int((nf+1)/2) * W/nf * 0.29' as='int((nf+2)/2) * W/nf * 0.29'
+ pd='2*int((nf+1)/2) * (W/nf + 0.29)' ps='2*int((nf+2)/2) * (W/nf + 0.29)' nrd='0.29 / W' nrs='0.29 / W'
+ sa=0 sb=0 sd=0 mult=1 m=1
**** begin user architecture code

.option wnflag=1
.param MC_SWITCH=0.0
.lib ~/skywater/skywater-pdk/libraries/sky130_fd_pr_ngspice/latest/models/sky130.lib.spice tt


.param W=64
.param L=8
.control
set wr_vecnames
set wr_singlescale
let code = 0
  while code < 128
    if code eq 0
      let b0 = 0
    else
      let b0 = code % 2
    end
    if floor(code / 2) eq 0
      let b1 = 0
    else
      let b1 = floor(code / 2) % 2
    end
    if floor(code / 4) eq 0
      let b2 = 0
    else
      let b2 = floor(code / 4) % 2
    end
    if floor(code / 8) eq 0
      let b3 = 0
    else
      let b3 = floor(code / 8) % 2
    end
    if floor(code / 16) eq 0
      let b4 = 0
    else
      let b4 = floor(code / 16) % 2
    end
    if floor(code / 32) eq 0
      let b5 = 0
    else
      let b5 = floor(code / 32) % 2
    end
    if floor(code / 64) eq 0
      let b6 = 0
    else
      let b6 = floor(code / 64) % 2
    end
    alter v0 $&b0
    alter v1 $&b1
    alter v2 $&b2
    alter v3 $&b3
    alter v4 $&b4
    alter v5 $&b5
    alter v6 $&b6
    save all
    op
    wrdata ~/Documents/current-output-dac-vlsi/simulations/dac_paper_sim.txt i(Vmeas) i(vb0) i(vb1)
+ i(vb2) i(vb3) i(vb4) i(vb5) i(vb6) i(Vout)
    if code eq 0
      set appendwrite
      set wr_vecnames = FALSE
    end
    let code = code + 1
  end
.endc

**** end user architecture code
**.ends

* expanding   symbol:  /home/madvlsi/Documents/current-output-dac-vlsi/schematics/mux.sym # of
*+ pins=4
** sym_path: /home/madvlsi/Documents/current-output-dac-vlsi/schematics/mux.sym
** sch_path: /home/madvlsi/Documents/current-output-dac-vlsi/schematics/mux.sch
.subckt mux A B Y S
*.ipin S
*.ipin A
*.opin Y
*.ipin B
XM1 net1 S GND GND sky130_fd_pr__nfet_01v8 L=0.15 W=1 nf=1 ad='int((nf+1)/2) * W/nf * 0.29' as='int((nf+2)/2) * W/nf * 0.29'
+ pd='2*int((nf+1)/2) * (W/nf + 0.29)' ps='2*int((nf+2)/2) * (W/nf + 0.29)' nrd='0.29 / W' nrs='0.29 / W'
+ sa=0 sb=0 sd=0 mult=1 m=1
XM2 net1 S VDD VDD sky130_fd_pr__pfet_01v8 L=0.15 W=1 nf=1 ad='int((nf+1)/2) * W/nf * 0.29' as='int((nf+2)/2) * W/nf * 0.29'
+ pd='2*int((nf+1)/2) * (W/nf + 0.29)' ps='2*int((nf+2)/2) * (W/nf + 0.29)' nrd='0.29 / W' nrs='0.29 / W'
+ sa=0 sb=0 sd=0 mult=1 m=1
XM3 Y S B GND sky130_fd_pr__nfet_01v8 L=0.15 W=1 nf=1 ad='int((nf+1)/2) * W/nf * 0.29' as='int((nf+2)/2) * W/nf * 0.29'
+ pd='2*int((nf+1)/2) * (W/nf + 0.29)' ps='2*int((nf+2)/2) * (W/nf + 0.29)' nrd='0.29 / W' nrs='0.29 / W'
+ sa=0 sb=0 sd=0 mult=1 m=1
XM4 A net1 Y GND sky130_fd_pr__nfet_01v8 L=0.15 W=1 nf=1 ad='int((nf+1)/2) * W/nf * 0.29' as='int((nf+2)/2) * W/nf * 0.29'
+ pd='2*int((nf+1)/2) * (W/nf + 0.29)' ps='2*int((nf+2)/2) * (W/nf + 0.29)' nrd='0.29 / W' nrs='0.29 / W'
+ sa=0 sb=0 sd=0 mult=1 m=1
.ends

.GLOBAL GND
.GLOBAL VDD
.end
